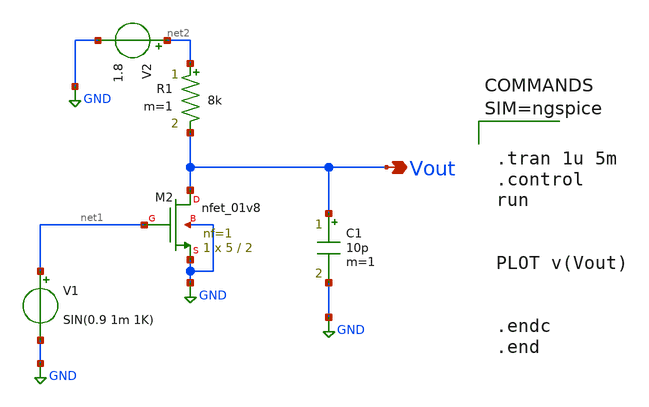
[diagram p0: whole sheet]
** sch_path: spice/mos_char.sch
**.subckt mos_char Vout
*.opin Vout
XM2 Vout net1 GND GND sky130_fd_pr__nfet_01v8 L=2 W=5 nf=1 ad='int((1 + 1)/2) * 5 / 1 * 0.29' as='int((1 + 2)/2) * 5 / 1 * 0.29'
+ pd='2*int((1 + 1)/2) * (5 / 1 + 0.29)' ps='2*int((1 + 2)/2) * (5 / 1 + 0.29)' nrd='0.29 / 5 ' nrs='0.29 / 5 '
+ sa=0 sb=0 sd=0 mult=1 m=1
C1 Vout GND 10p m=1
R1 net2 Vout 8k m=1
V1 net1 GND SIN(0.9 1m 1K)
V2 net2 GND 1.8
**** begin user architecture code

** opencircuitdesign pdks install
.lib $::SKYWATER_MODELS/sky130.lib.spice tt




.tran 1u 5m
.control
run


PLOT v(Vout)


.endc
.end






**** end user architecture code
**.ends
.GLOBAL GND
.end
